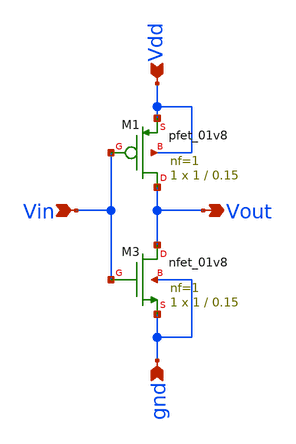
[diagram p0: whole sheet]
** sch_path: inv_vtc.sch
**.subckt inv_vtc Vin gnd Vdd Vout
*.ipin Vin
*.ipin gnd
*.ipin Vdd
*.opin Vout
XM3 Vout Vin gnd gnd sky130_fd_pr__nfet_01v8 L=0.15 W=1 nf=1 ad='int((nf+1)/2) * W/nf * 0.29' as='int((nf+2)/2) * W/nf * 0.29'
+ pd='2*int((nf+1)/2) * (W/nf + 0.29)' ps='2*int((nf+2)/2) * (W/nf + 0.29)' nrd='0.29 / W' nrs='0.29 / W'
+ sa=0 sb=0 sd=0 mult=1 m=1
XM1 Vout Vin Vdd Vdd sky130_fd_pr__pfet_01v8 L=0.15 W=1 nf=1 ad='int((nf+1)/2) * W/nf * 0.29' as='int((nf+2)/2) * W/nf * 0.29'
+ pd='2*int((nf+1)/2) * (W/nf + 0.29)' ps='2*int((nf+2)/2) * (W/nf + 0.29)' nrd='0.29 / W' nrs='0.29 / W'
+ sa=0 sb=0 sd=0 mult=1 m=1
**.ends
.end
